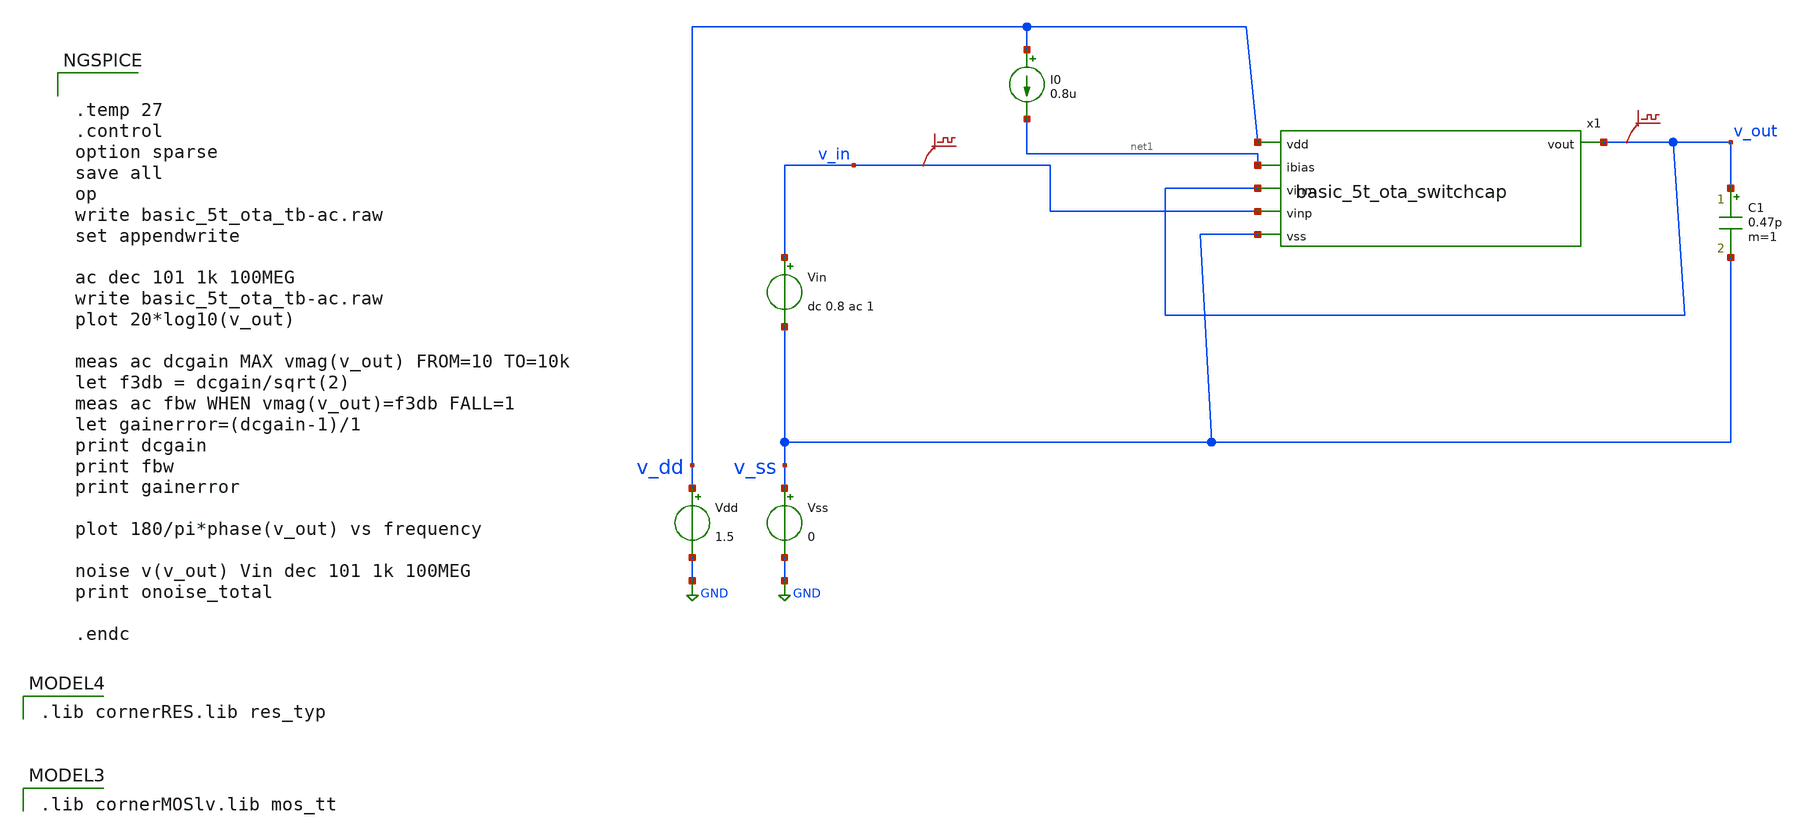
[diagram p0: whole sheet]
** sch_path: design/design_switch_cap/basic_5t_sc_ota_tb_ac.sch
**.subckt basic_5t_sc_ota_tb_ac
Vdd v_dd GND 1.5
Vss v_ss GND 0
C1 v_out v_ss 0.47p m=1
Vin v_in v_ss dc 0.8 ac 1
I0 v_dd net1 0.8u
.save v(v_in)
.save v(v_out)
x1 v_dd v_out net1 v_out v_in v_ss basic_5t_ota_switchcap
**** begin user architecture code


.temp 27
.control
option sparse
save all
op
write basic_5t_ota_tb-ac.raw
set appendwrite

ac dec 101 1k 100MEG
write basic_5t_ota_tb-ac.raw
plot 20*log10(v_out)

meas ac dcgain MAX vmag(v_out) FROM=10 TO=10k
let f3db = dcgain/sqrt(2)
meas ac fbw WHEN vmag(v_out)=f3db FALL=1
let gainerror=(dcgain-1)/1
print dcgain
print fbw
print gainerror

plot 180/pi*phase(v_out) vs frequency

noise v(v_out) Vin dec 101 1k 100MEG
print onoise_total

.endc


 .lib cornerMOSlv.lib mos_tt

 .lib cornerRES.lib res_typ

**** end user architecture code
**.ends

* expanding   symbol:  basic_5t_ota_switchcap.sym # of pins=6
** sym_path: zip_meiners/ic_design/design_switch_cap/basic_5t_ota_switchcap.sym
** sch_path: zip_meiners/ic_design/design_switch_cap/basic_5t_ota_switchcap.sch
.subckt basic_5t_ota_switchcap vdd vout ibias vinm vinp vss
*.ipin vss
*.ipin vdd
*.ipin ibias
*.ipin vinm
*.ipin vinp
*.opin vout
XM1 vout net1 vdd vdd sg13_lv_pmos w=0.16u l=0.5u ng=1 m=1 mm_ok=1
XM2 vout vinm net2 vss sg13_lv_nmos w=0.15u l=2u ng=1 m=1 mm_ok=1
XM3 net1 net1 vdd vdd sg13_lv_pmos w=0.16u l=0.5u ng=1 m=1 mm_ok=1
XM4 net1 vinp net2 vss sg13_lv_nmos w=0.15u l=2u ng=1 m=1 mm_ok=1
XM5 net2 net3 vss vss sg13_lv_nmos w=0.3u l=2u ng=1 m=1 mm_ok=1
XM6 net4 net3 vss vss sg13_lv_nmos w=0.15u l=2u ng=1 m=1 mm_ok=1
XM7 net3 net3 vss vss sg13_lv_nmos w=0.15u l=2u ng=1 m=1 mm_ok=1
XM9 vdd ibias net4 vss sg13_lv_nmos w=0.15u l=2u ng=1 m=1 mm_ok=1
XM8 ibias ibias net3 vss sg13_lv_nmos w=0.15u l=2u ng=1 m=1 mm_ok=1
.ends

.GLOBAL GND
.end
